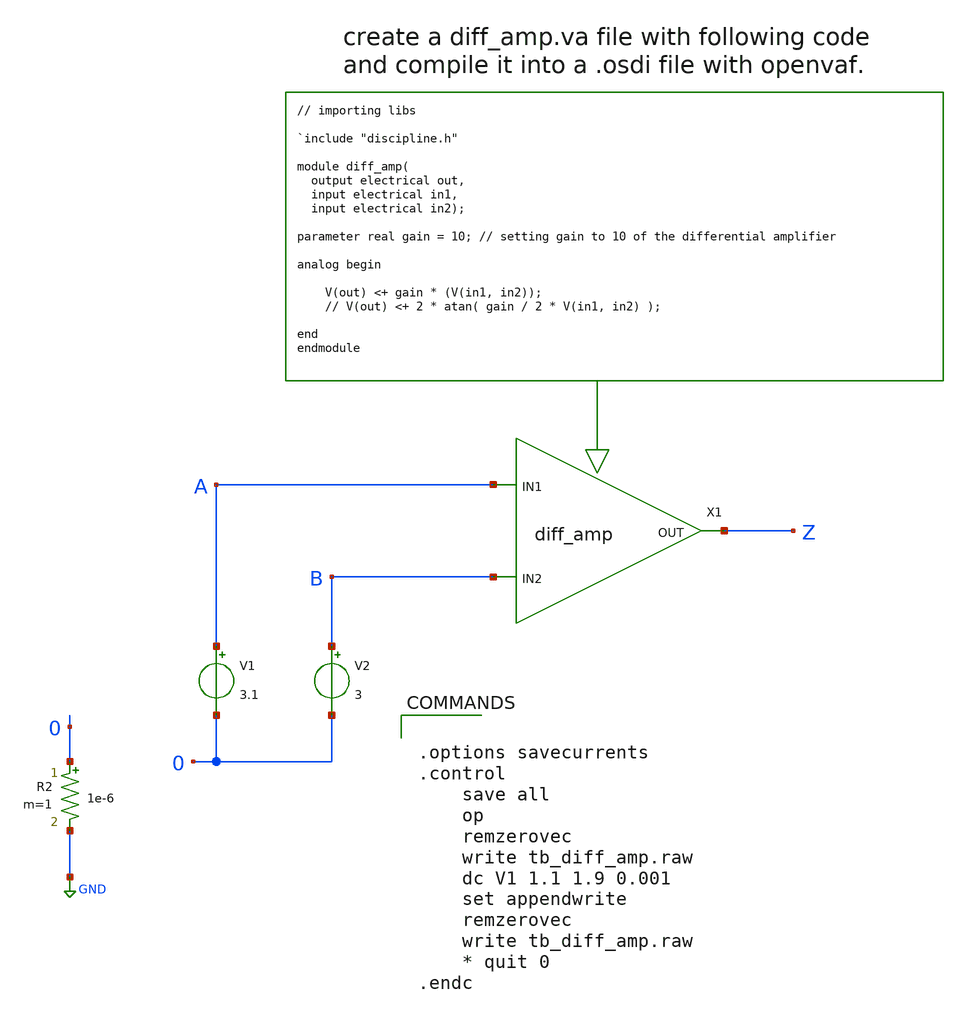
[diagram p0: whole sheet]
** sch_path: xsch/tb/tb_diff_amp.sch
**.subckt tb_diff_amp
XX1 diff_amp_cell
V1 A 0 3.1
V2 B 0 3
R2 0 GND 1e-6 m=1
**** begin user architecture code


.options savecurrents
.control
	save all
	op
	remzerovec
	write tb_diff_amp.raw
	dc V1 1.1 1.9 0.001
	set appendwrite
	remzerovec
	write tb_diff_amp.raw
	* quit 0
.endc


**** end user architecture code
**.ends
.GLOBAL GND
**** begin user architecture code

.subckt diff_amp_cell OUT IN1 IN2
N1 out in1 in2 diff_amp_model
.ends diff_amp_cell

.model diff_amp_model diff_amp

.control
* following line specifies the location for the .osdi file so ngspice can use it.
pre_osdi /home/vincef/projects/ttsky25b_tinychaos/xsch/veriloga/diff_amp.osdi
.endc

**** end user architecture code
.end
